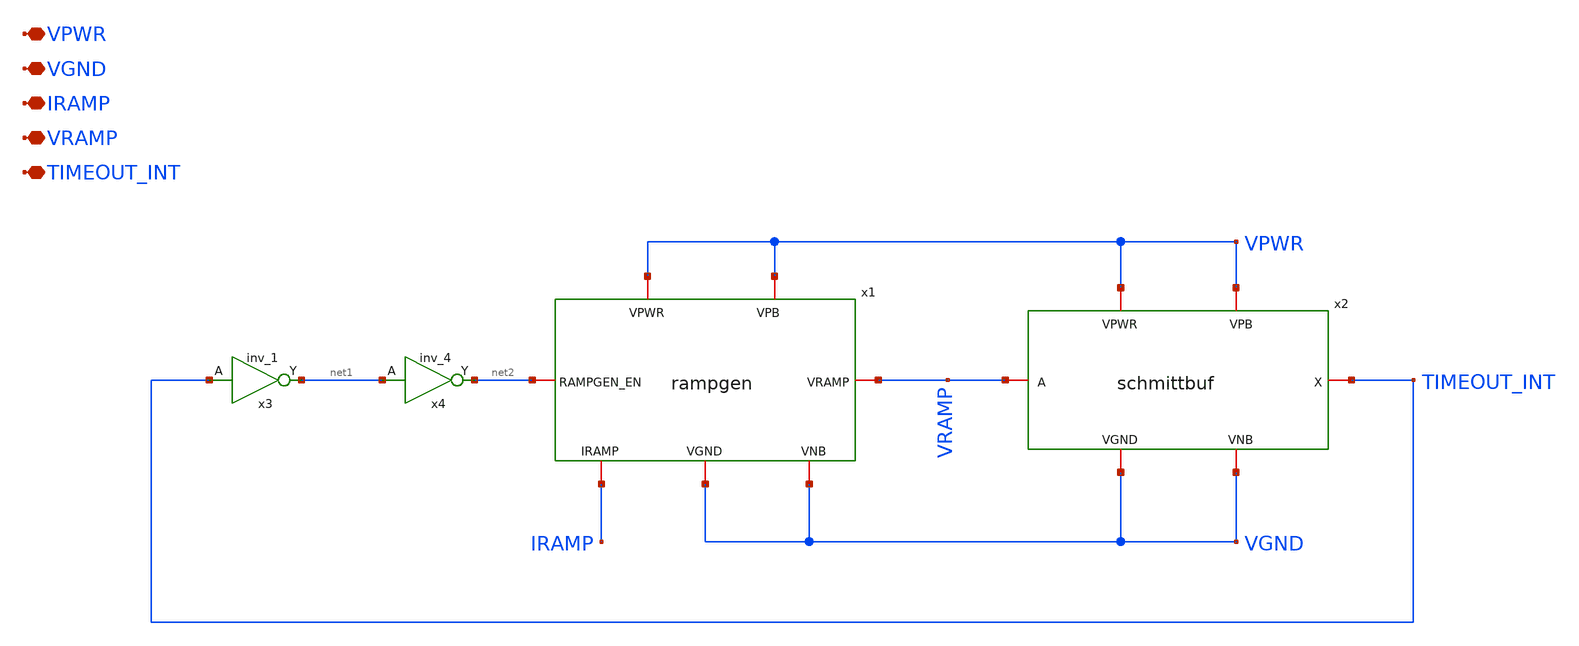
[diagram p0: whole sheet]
** sch_path: design/oscillator/oscillator.sch
**.subckt oscillator VPWR VGND IRAMP VRAMP TIMEOUT_INT
*.iopin VPWR
*.iopin VGND
*.iopin IRAMP
*.iopin VRAMP
*.iopin TIMEOUT_INT
x1 VPWR VGND VPWR VGND IRAMP VRAMP net2 rampgen
x2 VPWR VGND VPWR VGND VRAMP TIMEOUT_INT schmittbuf
x3 TIMEOUT_INT VGND VNB VPB VPWR net1 sky130_fd_sc_hvl__inv_1
x4 net1 VGND VNB VPB VPWR net2 sky130_fd_sc_hvl__inv_4
**.ends

* expanding   symbol:  design/oscillator/rampgen.sym # of pins=7
** sym_path: design/oscillator/rampgen.sym
** sch_path: design/oscillator/rampgen.sch
.subckt rampgen VPWR VGND VPB VNB IRAMP VRAMP RAMPGEN_EN
*.iopin VPWR
*.iopin VGND
*.iopin VPB
*.iopin VNB
*.iopin IRAMP
*.iopin VRAMP
*.iopin RAMPGEN_EN
XM1 IRAMP IRAMP VGND VNB sky130_fd_pr__nfet_g5v0d10v5 L=1 W=5 nf=1 ad='int((nf+1)/2) * W/nf * 0.29' as='int((nf+2)/2) * W/nf * 0.29'
+ pd='2*int((nf+1)/2) * (W/nf + 0.29)' ps='2*int((nf+2)/2) * (W/nf + 0.29)' nrd='0.29 / W' nrs='0.29 / W'
+ sa=0 sb=0 sd=0 mult=1 m=1
XM2 net3 IRAMP VGND VNB sky130_fd_pr__nfet_g5v0d10v5 L=1 W=5 nf=1 ad='int((nf+1)/2) * W/nf * 0.29' as='int((nf+2)/2) * W/nf * 0.29'
+ pd='2*int((nf+1)/2) * (W/nf + 0.29)' ps='2*int((nf+2)/2) * (W/nf + 0.29)' nrd='0.29 / W' nrs='0.29 / W'
+ sa=0 sb=0 sd=0 mult=1 m=1
XM3 net2 IRAMP VGND VNB sky130_fd_pr__nfet_g5v0d10v5 L=1 W=5 nf=1 ad='int((nf+1)/2) * W/nf * 0.29' as='int((nf+2)/2) * W/nf * 0.29'
+ pd='2*int((nf+1)/2) * (W/nf + 0.29)' ps='2*int((nf+2)/2) * (W/nf + 0.29)' nrd='0.29 / W' nrs='0.29 / W'
+ sa=0 sb=0 sd=0 mult=15 m=15
XM4 VRAMP RAMPGEN_EN net2 VNB sky130_fd_pr__nfet_g5v0d10v5 L=1 W=5 nf=1 ad='int((nf+1)/2) * W/nf * 0.29'
+ as='int((nf+2)/2) * W/nf * 0.29' pd='2*int((nf+1)/2) * (W/nf + 0.29)' ps='2*int((nf+2)/2) * (W/nf + 0.29)'
+ nrd='0.29 / W' nrs='0.29 / W' sa=0 sb=0 sd=0 mult=15 m=15
XM5 net3 net3 VPWR VPB sky130_fd_pr__pfet_g5v0d10v5 L=1 W=5 nf=1 ad='int((nf+1)/2) * W/nf * 0.29' as='int((nf+2)/2) * W/nf * 0.29'
+ pd='2*int((nf+1)/2) * (W/nf + 0.29)' ps='2*int((nf+2)/2) * (W/nf + 0.29)' nrd='0.29 / W' nrs='0.29 / W'
+ sa=0 sb=0 sd=0 mult=1 m=1
XM6 VRAMP RAMPGEN_EN net1 VPB sky130_fd_pr__pfet_g5v0d10v5 L=1 W=5 nf=1 ad='int((nf+1)/2) * W/nf * 0.29'
+ as='int((nf+2)/2) * W/nf * 0.29' pd='2*int((nf+1)/2) * (W/nf + 0.29)' ps='2*int((nf+2)/2) * (W/nf + 0.29)'
+ nrd='0.29 / W' nrs='0.29 / W' sa=0 sb=0 sd=0 mult=1 m=1
XM7 net1 net3 VPWR VPB sky130_fd_pr__pfet_g5v0d10v5 L=1 W=5 nf=1 ad='int((nf+1)/2) * W/nf * 0.29' as='int((nf+2)/2) * W/nf * 0.29'
+ pd='2*int((nf+1)/2) * (W/nf + 0.29)' ps='2*int((nf+2)/2) * (W/nf + 0.29)' nrd='0.29 / W' nrs='0.29 / W'
+ sa=0 sb=0 sd=0 mult=1 m=1
XC1 VRAMP VGND sky130_fd_pr__cap_mim_m3_1 W=20 L=26 MF=1 m=1
.ends


* expanding   symbol:  design/oscillator/schmittbuf.sym # of pins=6
** sym_path: design/oscillator/schmittbuf.sym
** sch_path: design/oscillator/schmittbuf.sch
.subckt schmittbuf VPWR VGND VPB VNB A X
*.iopin VPWR
*.iopin VGND
*.iopin VPB
*.iopin VNB
*.iopin A
*.iopin X
XM1 net1 A net2 VNB sky130_fd_pr__nfet_g5v0d10v5 L=1 W=5 nf=1 ad='int((nf+1)/2) * W/nf * 0.29' as='int((nf+2)/2) * W/nf * 0.29'
+ pd='2*int((nf+1)/2) * (W/nf + 0.29)' ps='2*int((nf+2)/2) * (W/nf + 0.29)' nrd='0.29 / W' nrs='0.29 / W'
+ sa=0 sb=0 sd=0 mult=1 m=1
XM8 net2 A VGND VNB sky130_fd_pr__nfet_g5v0d10v5 L=1 W=5 nf=1 ad='int((nf+1)/2) * W/nf * 0.29' as='int((nf+2)/2) * W/nf * 0.29'
+ pd='2*int((nf+1)/2) * (W/nf + 0.29)' ps='2*int((nf+2)/2) * (W/nf + 0.29)' nrd='0.29 / W' nrs='0.29 / W'
+ sa=0 sb=0 sd=0 mult=1 m=1
XM0 net1 A net3 VPB sky130_fd_pr__pfet_g5v0d10v5 L=1 W=5 nf=1 ad='int((nf+1)/2) * W/nf * 0.29' as='int((nf+2)/2) * W/nf * 0.29'
+ pd='2*int((nf+1)/2) * (W/nf + 0.29)' ps='2*int((nf+2)/2) * (W/nf + 0.29)' nrd='0.29 / W' nrs='0.29 / W'
+ sa=0 sb=0 sd=0 mult=2 m=2
XM4 net3 A VPWR VPB sky130_fd_pr__pfet_g5v0d10v5 L=1 W=5 nf=1 ad='int((nf+1)/2) * W/nf * 0.29' as='int((nf+2)/2) * W/nf * 0.29'
+ pd='2*int((nf+1)/2) * (W/nf + 0.29)' ps='2*int((nf+2)/2) * (W/nf + 0.29)' nrd='0.29 / W' nrs='0.29 / W'
+ sa=0 sb=0 sd=0 mult=2 m=2
XM7 VPWR net1 X VPB sky130_fd_pr__pfet_g5v0d10v5 L=1 W=5 nf=1 ad='int((nf+1)/2) * W/nf * 0.29' as='int((nf+2)/2) * W/nf * 0.29'
+ pd='2*int((nf+1)/2) * (W/nf + 0.29)' ps='2*int((nf+2)/2) * (W/nf + 0.29)' nrd='0.29 / W' nrs='0.29 / W'
+ sa=0 sb=0 sd=0 mult=2 m=2
XM6 VGND net1 X VNB sky130_fd_pr__nfet_g5v0d10v5 L=1 W=5 nf=1 ad='int((nf+1)/2) * W/nf * 0.29' as='int((nf+2)/2) * W/nf * 0.29'
+ pd='2*int((nf+1)/2) * (W/nf + 0.29)' ps='2*int((nf+2)/2) * (W/nf + 0.29)' nrd='0.29 / W' nrs='0.29 / W'
+ sa=0 sb=0 sd=0 mult=1 m=1
XM9 net4 net1 net3 VPB sky130_fd_pr__pfet_g5v0d10v5 L=0.5 W=5 nf=1 ad='int((nf+1)/2) * W/nf * 0.29' as='int((nf+2)/2) * W/nf * 0.29'
+ pd='2*int((nf+1)/2) * (W/nf + 0.29)' ps='2*int((nf+2)/2) * (W/nf + 0.29)' nrd='0.29 / W' nrs='0.29 / W'
+ sa=0 sb=0 sd=0 mult=4 m=4
XM5 net5 net1 net2 VNB sky130_fd_pr__nfet_g5v0d10v5 L=0.5 W=5 nf=1 ad='int((nf+1)/2) * W/nf * 0.29' as='int((nf+2)/2) * W/nf * 0.29'
+ pd='2*int((nf+1)/2) * (W/nf + 0.29)' ps='2*int((nf+2)/2) * (W/nf + 0.29)' nrd='0.29 / W' nrs='0.29 / W'
+ sa=0 sb=0 sd=0 mult=2 m=2
XR1 VGND net4 VNB sky130_fd_pr__res_generic_nd W=1 L=3 mult=1 m=1
XR2 net5 VPWR VPB sky130_fd_pr__res_generic_pd W=1 L=6 mult=1 m=1
.ends

.end
